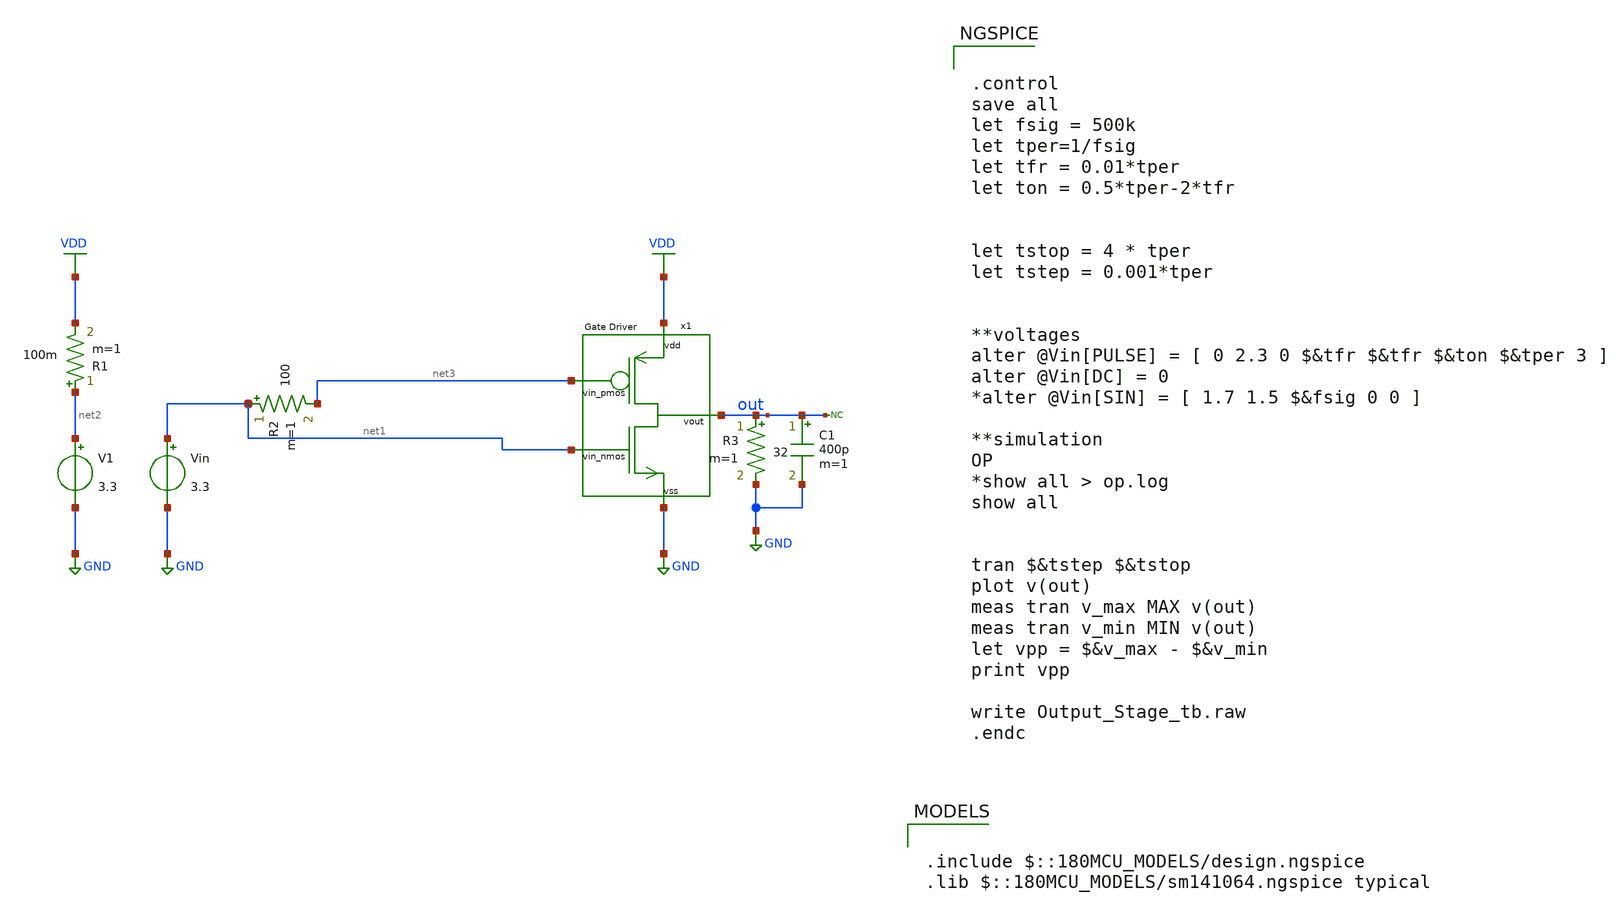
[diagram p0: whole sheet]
** sch_path: designs/libs/tb_analog/tb_Output_Stage/tb_Output_Stage.sch
**.subckt tb_Output_Stage
x1 VDD net3 out net1 GND Output_Stage_32_ohm
Vin net1 GND 3.3
V1 net2 GND 3.3
R1 net2 VDD 100m m=1
R2 net1 net3 100 m=1
* noconn out
R3 out GND 32 m=1
C1 out GND 400p m=1
**** begin user architecture code


.control
save all
let fsig = 500k
let tper=1/fsig
let tfr = 0.01*tper
let ton = 0.5*tper-2*tfr


let tstop = 4 * tper
let tstep = 0.001*tper


**voltages
alter @Vin[PULSE] = [ 0 2.3 0 $&tfr $&tfr $&ton $&tper 3 ]
alter @Vin[DC] = 0
*alter @Vin[SIN] = [ 1.7 1.5 $&fsig 0 0 ]

**simulation
OP
*show all > op.log
show all


tran $&tstep $&tstop
plot v(out)
meas tran v_max MAX v(out)
meas tran v_min MIN v(out)
let vpp = $&v_max - $&v_min
print vpp

write Output_Stage_tb.raw
.endc



.include $::180MCU_MODELS/design.ngspice
.lib $::180MCU_MODELS/sm141064.ngspice typical

**** end user architecture code
**.ends

* expanding   symbol:  libs/core_analog/Output_Stage/Output_Stage_32_ohm.sym # of pins=5
** sym_path: designs/libs/core_analog/Output_Stage/Output_Stage_32_ohm.sym
** sch_path: designs/libs/core_analog/Output_Stage/Output_Stage_32_ohm.sch
.subckt Output_Stage_32_ohm vdd vin_pmos vout vin_nmos vss
*.ipin vin_pmos
*.ipin vdd
*.ipin vss
*.opin vout
*.ipin vin_nmos
XM1 vout vin_pmos vdd vdd pfet_03v3 L=0.28u W=5u nf=2 ad='int((nf+1)/2) * W/nf * 0.18u' as='int((nf+2)/2) * W/nf * 0.18u'
+ pd='2*int((nf+1)/2) * (W/nf + 0.18u)' ps='2*int((nf+2)/2) * (W/nf + 0.18u)' nrd='0.18u / W' nrs='0.18u / W'
+ sa=0 sb=0 sd=0 m=5504
XM2 vout vin_nmos vss vss nfet_03v3 L=0.28u W=5u nf=2 ad='int((nf+1)/2) * W/nf * 0.18u' as='int((nf+2)/2) * W/nf * 0.18u'
+ pd='2*int((nf+1)/2) * (W/nf + 0.18u)' ps='2*int((nf+2)/2) * (W/nf + 0.18u)' nrd='0.18u / W' nrs='0.18u / W'
+ sa=0 sb=0 sd=0 m=1304
.ends

.GLOBAL VDD
.GLOBAL GND
.end
